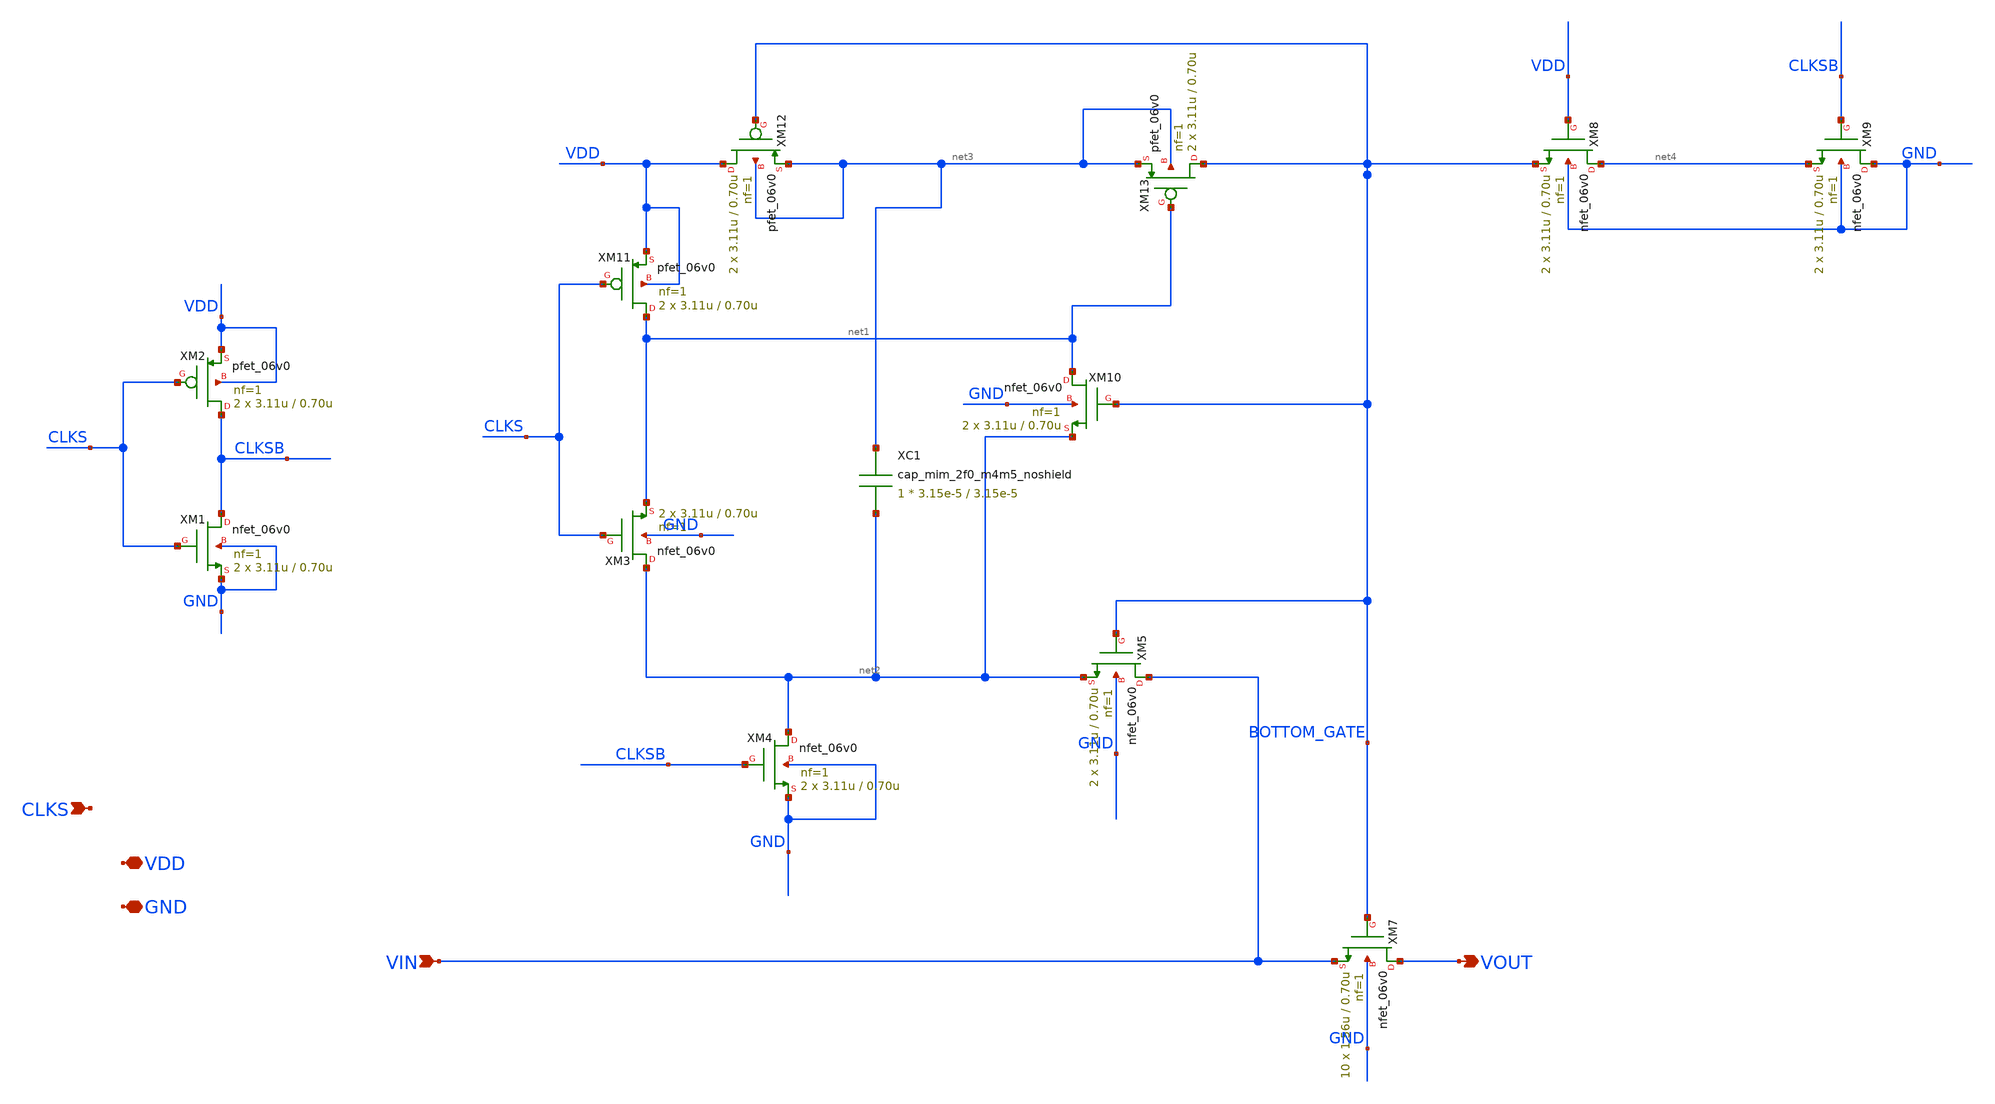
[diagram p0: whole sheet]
** sch_path: verification/a44_r2/01_CURRENT_CIRCUIT_FILES/xschem/SWITCH_BOOT_SP.sch
**.subckt SWITCH_BOOT_SP CLKS VIN VOUT VDD GND
*.ipin CLKS
*.ipin VIN
*.opin VOUT
*.iopin VDD
*.iopin GND
XM1 CLKSB CLKS GND GND nfet_06v0 L=0.70u W=3.11u nf=1 ad='int((nf+1)/2) * W/nf * 0.18u' as='int((nf+2)/2) * W/nf * 0.18u'
+ pd='2*int((nf+1)/2) * (W/nf + 0.18u)' ps='2*int((nf+2)/2) * (W/nf + 0.18u)' nrd='0.18u / W' nrs='0.18u / W'
+ sa=0 sb=0 sd=0 m=2
XM2 CLKSB CLKS VDD VDD pfet_06v0 L=0.70u W=3.11u nf=1 ad='int((nf+1)/2) * W/nf * 0.18u' as='int((nf+2)/2) * W/nf * 0.18u'
+ pd='2*int((nf+1)/2) * (W/nf + 0.18u)' ps='2*int((nf+2)/2) * (W/nf + 0.18u)' nrd='0.18u / W' nrs='0.18u / W'
+ sa=0 sb=0 sd=0 m=2
XM3 net2 CLKS net1 GND nfet_06v0 L=0.70u W=3.11u nf=1 ad='int((nf+1)/2) * W/nf * 0.18u' as='int((nf+2)/2) * W/nf * 0.18u'
+ pd='2*int((nf+1)/2) * (W/nf + 0.18u)' ps='2*int((nf+2)/2) * (W/nf + 0.18u)' nrd='0.18u / W' nrs='0.18u / W'
+ sa=0 sb=0 sd=0 m=2
XM4 net2 CLKSB GND GND nfet_06v0 L=0.70u W=3.11u nf=1 ad='int((nf+1)/2) * W/nf * 0.18u' as='int((nf+2)/2) * W/nf * 0.18u'
+ pd='2*int((nf+1)/2) * (W/nf + 0.18u)' ps='2*int((nf+2)/2) * (W/nf + 0.18u)' nrd='0.18u / W' nrs='0.18u / W'
+ sa=0 sb=0 sd=0 m=2
XM5 VIN BOTTOM_GATE net2 GND nfet_06v0 L=0.70u W=3.11u nf=1 ad='int((nf+1)/2) * W/nf * 0.18u' as='int((nf+2)/2) * W/nf * 0.18u'
+ pd='2*int((nf+1)/2) * (W/nf + 0.18u)' ps='2*int((nf+2)/2) * (W/nf + 0.18u)' nrd='0.18u / W' nrs='0.18u / W'
+ sa=0 sb=0 sd=0 m=2
XM7 VOUT BOTTOM_GATE VIN GND nfet_06v0 L=0.70u W=1.56u nf=1 ad='int((nf+1)/2) * W/nf * 0.18u' as='int((nf+2)/2) * W/nf * 0.18u'
+ pd='2*int((nf+1)/2) * (W/nf + 0.18u)' ps='2*int((nf+2)/2) * (W/nf + 0.18u)' nrd='0.18u / W' nrs='0.18u / W'
+ sa=0 sb=0 sd=0 m=10
XM8 net4 VDD BOTTOM_GATE GND nfet_06v0 L=0.70u W=3.11u nf=1 ad='int((nf+1)/2) * W/nf * 0.18u' as='int((nf+2)/2) * W/nf * 0.18u'
+ pd='2*int((nf+1)/2) * (W/nf + 0.18u)' ps='2*int((nf+2)/2) * (W/nf + 0.18u)' nrd='0.18u / W' nrs='0.18u / W'
+ sa=0 sb=0 sd=0 m=2
XM9 GND CLKSB net4 GND nfet_06v0 L=0.70u W=3.11u nf=1 ad='int((nf+1)/2) * W/nf * 0.18u' as='int((nf+2)/2) * W/nf * 0.18u'
+ pd='2*int((nf+1)/2) * (W/nf + 0.18u)' ps='2*int((nf+2)/2) * (W/nf + 0.18u)' nrd='0.18u / W' nrs='0.18u / W'
+ sa=0 sb=0 sd=0 m=2
XM10 net1 BOTTOM_GATE net2 GND nfet_06v0 L=0.70u W=3.11u nf=1 ad='int((nf+1)/2) * W/nf * 0.18u' as='int((nf+2)/2) * W/nf * 0.18u'
+ pd='2*int((nf+1)/2) * (W/nf + 0.18u)' ps='2*int((nf+2)/2) * (W/nf + 0.18u)' nrd='0.18u / W' nrs='0.18u / W'
+ sa=0 sb=0 sd=0 m=2
XM11 net1 CLKS VDD VDD pfet_06v0 L=0.70u W=3.11u nf=1 ad='int((nf+1)/2) * W/nf * 0.18u' as='int((nf+2)/2) * W/nf * 0.18u'
+ pd='2*int((nf+1)/2) * (W/nf + 0.18u)' ps='2*int((nf+2)/2) * (W/nf + 0.18u)' nrd='0.18u / W' nrs='0.18u / W'
+ sa=0 sb=0 sd=0 m=2
XM12 VDD BOTTOM_GATE net3 net3 pfet_06v0 L=0.70u W=3.11u nf=1 ad='int((nf+1)/2) * W/nf * 0.18u' as='int((nf+2)/2) * W/nf * 0.18u'
+ pd='2*int((nf+1)/2) * (W/nf + 0.18u)' ps='2*int((nf+2)/2) * (W/nf + 0.18u)' nrd='0.18u / W' nrs='0.18u / W'
+ sa=0 sb=0 sd=0 m=2
XM13 BOTTOM_GATE net1 net3 net3 pfet_06v0 L=0.70u W=3.11u nf=1 ad='int((nf+1)/2) * W/nf * 0.18u' as='int((nf+2)/2) * W/nf * 0.18u'
+ pd='2*int((nf+1)/2) * (W/nf + 0.18u)' ps='2*int((nf+2)/2) * (W/nf + 0.18u)' nrd='0.18u / W' nrs='0.18u / W'
+ sa=0 sb=0 sd=0 m=2
XC1 net3 net2 cap_mim_2f0_m4m5_noshield c_width=3.15e-5 c_length=3.15e-5 m=1
**.ends
.end
